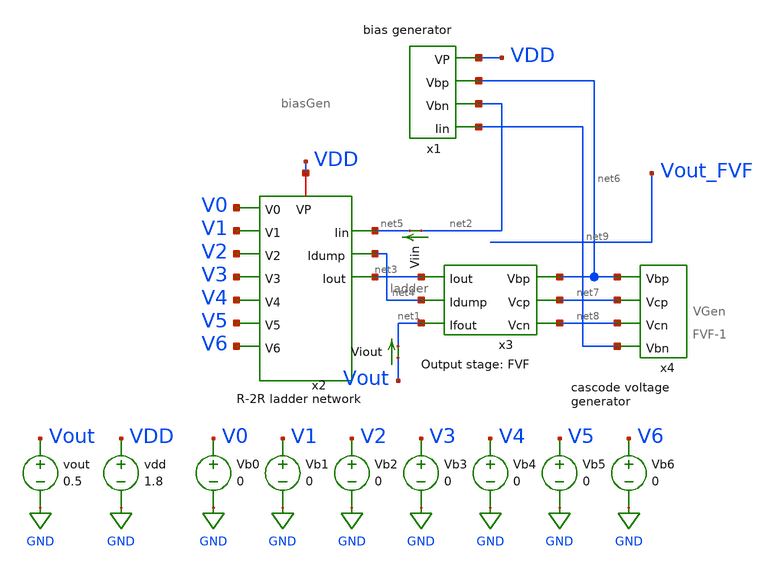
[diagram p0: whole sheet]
** sch_path: xschem/old_files/mp4_dac_simulation_mc.sch
**.subckt mp4_dac_simulation_mc
Vb1 V1 GND 0
Vb2 V2 GND 0
Vb3 V3 GND 0
Vb4 V4 GND 0
Vb5 V5 GND 0
Vb6 V6 GND 0
Vb0 V0 GND 0
vdd VDD GND 1.8
vout Vout GND 0.5
Viout Vout net1 0
.save i(viout)
Viin net2 net5 0
.save i(viin)
x2 V0 VDD net4 net3 net5 V1 V2 V3 V4 V5 V6 ladder
x1 net6 net9 net2 VDD biasGen
x3 net6 net7 net3 net8 net1 net4 FVF-1
x4 net6 net8 net7 net9 VGen
**** begin user architecture code

.option wnflag=1
.param MC_SWITCH=1.0
.lib ~/skywater/skywater-pdk/libraries/sky130_fd_pr_ngspice/latest/models/sky130.lib.spice tt



.control
  set wr_singlescale
  let runs = 10
  let run = 1
  while run <= runs
  set appendwrite = FALSE
  set wr_vecnames
  let code = 0
   while code < 128
    if code eq 0
      let b0 = 0
    else
      let b0 = code % 2
    end
    if floor(code / 2) eq 0
      let b1 = 0
    else
      let b1 = floor(code / 2) % 2
    end
    if floor(code / 4) eq 0
      let b2 = 0
    else
      let b2 = floor(code / 4) % 2
    end
    if floor(code / 8) eq 0
      let b3 = 0
    else
      let b3 = floor(code / 8) % 2
    end
    if floor(code / 16) eq 0
      let b4 = 0
    else
      let b4 = floor(code / 16) % 2
    end
    if floor(code / 32) eq 0
      let b5 = 0
    else
      let b5 = floor(code / 32) % 2
    end
    if floor(code / 64) eq 0
      let b6 = 0
    else
      let b6 = floor(code / 64) % 2
    end
    alter Vb0 1.8*$&b0
    alter Vb1 1.8*$&b1
    alter Vb2 1.8*$&b2
    alter Vb3 1.8*$&b3
    alter Vb4 1.8*$&b4
    alter Vb5 1.8*$&b5
    alter Vb6 1.8*$&b6
    save all
    op
    wrdata ~/Documents/DAC-VLSI/simulation_results/mc/dac_simulation_mc_24_12_{$&run}.txt v(b0) v(b1)
+ v(b2) v(b3) v(b4) v(b5) v(b6) v(Vout_FVF) v(vout) i(Viin) i(Viout)
    if code eq 0
      set appendwrite
      set wr_vecnames = FALSE
    end
    let code = code + 1
  end
  reset
  let run = run + 1
  end
  quit
.endc


**** end user architecture code
**.ends

* expanding   symbol:  ./ladder.sym # of pins=11
** sym_path: xschem/ladder.sym
** sch_path: xschem/ladder.sch
.subckt ladder V0 VP Idump Iout Iin V1 V2 V3 V4 V5 V6
*.ipin V6
*.ipin V5
*.ipin V4
*.ipin V3
*.ipin V2
*.ipin V1
*.ipin V0
*.iopin VP
*.iopin Iin
*.opin Idump
*.opin Iout
XM1 Iin VP net1 GND sky130_fd_pr__nfet_01v8 L=4 W=12 nf=1 ad='int((nf+1)/2) * W/nf * 0.29' as='int((nf+2)/2) * W/nf * 0.29'
+ pd='2*int((nf+1)/2) * (W/nf + 0.29)' ps='2*int((nf+2)/2) * (W/nf + 0.29)' nrd='0.29 / W' nrs='0.29 / W'
+ sa=0 sb=0 sd=0 mult=1 m=1
XM3 Iin VP net2 GND sky130_fd_pr__nfet_01v8 L=4 W=12 nf=1 ad='int((nf+1)/2) * W/nf * 0.29' as='int((nf+2)/2) * W/nf * 0.29'
+ pd='2*int((nf+1)/2) * (W/nf + 0.29)' ps='2*int((nf+2)/2) * (W/nf + 0.29)' nrd='0.29 / W' nrs='0.29 / W'
+ sa=0 sb=0 sd=0 mult=1 m=1
XM5 net2 VP net3 GND sky130_fd_pr__nfet_01v8 L=4 W=12 nf=1 ad='int((nf+1)/2) * W/nf * 0.29' as='int((nf+2)/2) * W/nf * 0.29'
+ pd='2*int((nf+1)/2) * (W/nf + 0.29)' ps='2*int((nf+2)/2) * (W/nf + 0.29)' nrd='0.29 / W' nrs='0.29 / W'
+ sa=0 sb=0 sd=0 mult=1 m=1
XM7 net2 VP net4 GND sky130_fd_pr__nfet_01v8 L=4 W=12 nf=1 ad='int((nf+1)/2) * W/nf * 0.29' as='int((nf+2)/2) * W/nf * 0.29'
+ pd='2*int((nf+1)/2) * (W/nf + 0.29)' ps='2*int((nf+2)/2) * (W/nf + 0.29)' nrd='0.29 / W' nrs='0.29 / W'
+ sa=0 sb=0 sd=0 mult=1 m=1
XM6 net3 V5 Iout GND sky130_fd_pr__nfet_01v8 L=4 W=12 nf=1 ad='int((nf+1)/2) * W/nf * 0.29' as='int((nf+2)/2) * W/nf * 0.29'
+ pd='2*int((nf+1)/2) * (W/nf + 0.29)' ps='2*int((nf+2)/2) * (W/nf + 0.29)' nrd='0.29 / W' nrs='0.29 / W'
+ sa=0 sb=0 sd=0 mult=1 m=1
XM8 net3 net16 Idump GND sky130_fd_pr__nfet_01v8 L=4 W=12 nf=1 ad='int((nf+1)/2) * W/nf * 0.29' as='int((nf+2)/2) * W/nf * 0.29'
+ pd='2*int((nf+1)/2) * (W/nf + 0.29)' ps='2*int((nf+2)/2) * (W/nf + 0.29)' nrd='0.29 / W' nrs='0.29 / W'
+ sa=0 sb=0 sd=0 mult=1 m=1
XM2 net1 V6 Iout GND sky130_fd_pr__nfet_01v8 L=4 W=12 nf=1 ad='int((nf+1)/2) * W/nf * 0.29' as='int((nf+2)/2) * W/nf * 0.29'
+ pd='2*int((nf+1)/2) * (W/nf + 0.29)' ps='2*int((nf+2)/2) * (W/nf + 0.29)' nrd='0.29 / W' nrs='0.29 / W'
+ sa=0 sb=0 sd=0 mult=1 m=1
XM4 net1 net15 Idump GND sky130_fd_pr__nfet_01v8 L=4 W=12 nf=1 ad='int((nf+1)/2) * W/nf * 0.29' as='int((nf+2)/2) * W/nf * 0.29'
+ pd='2*int((nf+1)/2) * (W/nf + 0.29)' ps='2*int((nf+2)/2) * (W/nf + 0.29)' nrd='0.29 / W' nrs='0.29 / W'
+ sa=0 sb=0 sd=0 mult=1 m=1
XM9 net4 VP net5 GND sky130_fd_pr__nfet_01v8 L=4 W=12 nf=1 ad='int((nf+1)/2) * W/nf * 0.29' as='int((nf+2)/2) * W/nf * 0.29'
+ pd='2*int((nf+1)/2) * (W/nf + 0.29)' ps='2*int((nf+2)/2) * (W/nf + 0.29)' nrd='0.29 / W' nrs='0.29 / W'
+ sa=0 sb=0 sd=0 mult=1 m=1
XM11 net4 VP net6 GND sky130_fd_pr__nfet_01v8 L=4 W=12 nf=1 ad='int((nf+1)/2) * W/nf * 0.29' as='int((nf+2)/2) * W/nf * 0.29'
+ pd='2*int((nf+1)/2) * (W/nf + 0.29)' ps='2*int((nf+2)/2) * (W/nf + 0.29)' nrd='0.29 / W' nrs='0.29 / W'
+ sa=0 sb=0 sd=0 mult=1 m=1
XM10 net5 V4 Iout GND sky130_fd_pr__nfet_01v8 L=4 W=12 nf=1 ad='int((nf+1)/2) * W/nf * 0.29' as='int((nf+2)/2) * W/nf * 0.29'
+ pd='2*int((nf+1)/2) * (W/nf + 0.29)' ps='2*int((nf+2)/2) * (W/nf + 0.29)' nrd='0.29 / W' nrs='0.29 / W'
+ sa=0 sb=0 sd=0 mult=1 m=1
XM12 net5 net17 Idump GND sky130_fd_pr__nfet_01v8 L=4 W=12 nf=1 ad='int((nf+1)/2) * W/nf * 0.29' as='int((nf+2)/2) * W/nf * 0.29'
+ pd='2*int((nf+1)/2) * (W/nf + 0.29)' ps='2*int((nf+2)/2) * (W/nf + 0.29)' nrd='0.29 / W' nrs='0.29 / W'
+ sa=0 sb=0 sd=0 mult=1 m=1
XM13 net6 VP net7 GND sky130_fd_pr__nfet_01v8 L=4 W=12 nf=1 ad='int((nf+1)/2) * W/nf * 0.29' as='int((nf+2)/2) * W/nf * 0.29'
+ pd='2*int((nf+1)/2) * (W/nf + 0.29)' ps='2*int((nf+2)/2) * (W/nf + 0.29)' nrd='0.29 / W' nrs='0.29 / W'
+ sa=0 sb=0 sd=0 mult=1 m=1
XM15 net6 VP net8 GND sky130_fd_pr__nfet_01v8 L=4 W=12 nf=1 ad='int((nf+1)/2) * W/nf * 0.29' as='int((nf+2)/2) * W/nf * 0.29'
+ pd='2*int((nf+1)/2) * (W/nf + 0.29)' ps='2*int((nf+2)/2) * (W/nf + 0.29)' nrd='0.29 / W' nrs='0.29 / W'
+ sa=0 sb=0 sd=0 mult=1 m=1
XM14 net7 V3 Iout GND sky130_fd_pr__nfet_01v8 L=4 W=12 nf=1 ad='int((nf+1)/2) * W/nf * 0.29' as='int((nf+2)/2) * W/nf * 0.29'
+ pd='2*int((nf+1)/2) * (W/nf + 0.29)' ps='2*int((nf+2)/2) * (W/nf + 0.29)' nrd='0.29 / W' nrs='0.29 / W'
+ sa=0 sb=0 sd=0 mult=1 m=1
XM16 net7 net18 Idump GND sky130_fd_pr__nfet_01v8 L=4 W=12 nf=1 ad='int((nf+1)/2) * W/nf * 0.29' as='int((nf+2)/2) * W/nf * 0.29'
+ pd='2*int((nf+1)/2) * (W/nf + 0.29)' ps='2*int((nf+2)/2) * (W/nf + 0.29)' nrd='0.29 / W' nrs='0.29 / W'
+ sa=0 sb=0 sd=0 mult=1 m=1
XM17 net8 VP net9 GND sky130_fd_pr__nfet_01v8 L=4 W=12 nf=1 ad='int((nf+1)/2) * W/nf * 0.29' as='int((nf+2)/2) * W/nf * 0.29'
+ pd='2*int((nf+1)/2) * (W/nf + 0.29)' ps='2*int((nf+2)/2) * (W/nf + 0.29)' nrd='0.29 / W' nrs='0.29 / W'
+ sa=0 sb=0 sd=0 mult=1 m=1
XM19 net8 VP net10 GND sky130_fd_pr__nfet_01v8 L=4 W=12 nf=1 ad='int((nf+1)/2) * W/nf * 0.29' as='int((nf+2)/2) * W/nf * 0.29'
+ pd='2*int((nf+1)/2) * (W/nf + 0.29)' ps='2*int((nf+2)/2) * (W/nf + 0.29)' nrd='0.29 / W' nrs='0.29 / W'
+ sa=0 sb=0 sd=0 mult=1 m=1
XM18 net9 V2 Iout GND sky130_fd_pr__nfet_01v8 L=4 W=12 nf=1 ad='int((nf+1)/2) * W/nf * 0.29' as='int((nf+2)/2) * W/nf * 0.29'
+ pd='2*int((nf+1)/2) * (W/nf + 0.29)' ps='2*int((nf+2)/2) * (W/nf + 0.29)' nrd='0.29 / W' nrs='0.29 / W'
+ sa=0 sb=0 sd=0 mult=1 m=1
XM20 net9 net19 Idump GND sky130_fd_pr__nfet_01v8 L=4 W=12 nf=1 ad='int((nf+1)/2) * W/nf * 0.29' as='int((nf+2)/2) * W/nf * 0.29'
+ pd='2*int((nf+1)/2) * (W/nf + 0.29)' ps='2*int((nf+2)/2) * (W/nf + 0.29)' nrd='0.29 / W' nrs='0.29 / W'
+ sa=0 sb=0 sd=0 mult=1 m=1
XM21 net10 VP net11 GND sky130_fd_pr__nfet_01v8 L=4 W=12 nf=1 ad='int((nf+1)/2) * W/nf * 0.29' as='int((nf+2)/2) * W/nf * 0.29'
+ pd='2*int((nf+1)/2) * (W/nf + 0.29)' ps='2*int((nf+2)/2) * (W/nf + 0.29)' nrd='0.29 / W' nrs='0.29 / W'
+ sa=0 sb=0 sd=0 mult=1 m=1
XM23 net10 VP net12 GND sky130_fd_pr__nfet_01v8 L=4 W=12 nf=1 ad='int((nf+1)/2) * W/nf * 0.29' as='int((nf+2)/2) * W/nf * 0.29'
+ pd='2*int((nf+1)/2) * (W/nf + 0.29)' ps='2*int((nf+2)/2) * (W/nf + 0.29)' nrd='0.29 / W' nrs='0.29 / W'
+ sa=0 sb=0 sd=0 mult=1 m=1
XM22 net11 V1 Iout GND sky130_fd_pr__nfet_01v8 L=4 W=12 nf=1 ad='int((nf+1)/2) * W/nf * 0.29' as='int((nf+2)/2) * W/nf * 0.29'
+ pd='2*int((nf+1)/2) * (W/nf + 0.29)' ps='2*int((nf+2)/2) * (W/nf + 0.29)' nrd='0.29 / W' nrs='0.29 / W'
+ sa=0 sb=0 sd=0 mult=1 m=1
XM24 net11 net20 Idump GND sky130_fd_pr__nfet_01v8 L=4 W=12 nf=1 ad='int((nf+1)/2) * W/nf * 0.29' as='int((nf+2)/2) * W/nf * 0.29'
+ pd='2*int((nf+1)/2) * (W/nf + 0.29)' ps='2*int((nf+2)/2) * (W/nf + 0.29)' nrd='0.29 / W' nrs='0.29 / W'
+ sa=0 sb=0 sd=0 mult=1 m=1
XM25 net12 VP net13 GND sky130_fd_pr__nfet_01v8 L=4 W=12 nf=1 ad='int((nf+1)/2) * W/nf * 0.29' as='int((nf+2)/2) * W/nf * 0.29'
+ pd='2*int((nf+1)/2) * (W/nf + 0.29)' ps='2*int((nf+2)/2) * (W/nf + 0.29)' nrd='0.29 / W' nrs='0.29 / W'
+ sa=0 sb=0 sd=0 mult=1 m=1
XM27 net12 VP net14 GND sky130_fd_pr__nfet_01v8 L=4 W=12 nf=1 ad='int((nf+1)/2) * W/nf * 0.29' as='int((nf+2)/2) * W/nf * 0.29'
+ pd='2*int((nf+1)/2) * (W/nf + 0.29)' ps='2*int((nf+2)/2) * (W/nf + 0.29)' nrd='0.29 / W' nrs='0.29 / W'
+ sa=0 sb=0 sd=0 mult=1 m=1
XM26 net13 V0 Iout GND sky130_fd_pr__nfet_01v8 L=4 W=12 nf=1 ad='int((nf+1)/2) * W/nf * 0.29' as='int((nf+2)/2) * W/nf * 0.29'
+ pd='2*int((nf+1)/2) * (W/nf + 0.29)' ps='2*int((nf+2)/2) * (W/nf + 0.29)' nrd='0.29 / W' nrs='0.29 / W'
+ sa=0 sb=0 sd=0 mult=1 m=1
XM28 net13 net21 Idump GND sky130_fd_pr__nfet_01v8 L=4 W=12 nf=1 ad='int((nf+1)/2) * W/nf * 0.29' as='int((nf+2)/2) * W/nf * 0.29'
+ pd='2*int((nf+1)/2) * (W/nf + 0.29)' ps='2*int((nf+2)/2) * (W/nf + 0.29)' nrd='0.29 / W' nrs='0.29 / W'
+ sa=0 sb=0 sd=0 mult=1 m=1
XM29 net14 VP Idump GND sky130_fd_pr__nfet_01v8 L=4 W=12 nf=1 ad='int((nf+1)/2) * W/nf * 0.29' as='int((nf+2)/2) * W/nf * 0.29'
+ pd='2*int((nf+1)/2) * (W/nf + 0.29)' ps='2*int((nf+2)/2) * (W/nf + 0.29)' nrd='0.29 / W' nrs='0.29 / W'
+ sa=0 sb=0 sd=0 mult=1 m=1
x1 net15 V6 inverter
x2 net16 V5 inverter
x3 net17 V4 inverter
x4 net18 V3 inverter
x5 net19 V2 inverter
x6 net20 V1 inverter
x7 net21 V0 inverter
.ends


* expanding   symbol:  /home/madvlsi/Documents/DAC-VLSI/xschem/biasGen.sym # of pins=4
** sym_path: xschem/biasGen.sym
** sch_path: xschem/biasGen.sch
.subckt biasGen Vbp Iin Vbn VP
*.opin Iin
*.ipin VP
*.opin Vbp
*.opin Vbn
XM1 Vbn Vbn GND GND sky130_fd_pr__nfet_01v8 L=4 W=24 nf=1 ad='int((nf+1)/2) * W/nf * 0.29' as='int((nf+2)/2) * W/nf * 0.29'
+ pd='2*int((nf+1)/2) * (W/nf + 0.29)' ps='2*int((nf+2)/2) * (W/nf + 0.29)' nrd='0.29 / W' nrs='0.29 / W'
+ sa=0 sb=0 sd=0 mult=1 m=1
XM2 GND Vbn Vbp GND sky130_fd_pr__nfet_01v8 L=4 W=24 nf=1 ad='int((nf+1)/2) * W/nf * 0.29' as='int((nf+2)/2) * W/nf * 0.29'
+ pd='2*int((nf+1)/2) * (W/nf + 0.29)' ps='2*int((nf+2)/2) * (W/nf + 0.29)' nrd='0.29 / W' nrs='0.29 / W'
+ sa=0 sb=0 sd=0 mult=1 m=1
XM3 net1 net2 GND GND sky130_fd_pr__nfet_01v8 L=4 W=24 nf=1 ad='int((nf+1)/2) * W/nf * 0.29' as='int((nf+2)/2) * W/nf * 0.29'
+ pd='2*int((nf+1)/2) * (W/nf + 0.29)' ps='2*int((nf+2)/2) * (W/nf + 0.29)' nrd='0.29 / W' nrs='0.29 / W'
+ sa=0 sb=0 sd=0 mult=1 m=1
XM4 net13 net2 net2 GND sky130_fd_pr__nfet_01v8 L=4 W=24 nf=1 ad='int((nf+1)/2) * W/nf * 0.29' as='int((nf+2)/2) * W/nf * 0.29'
+ pd='2*int((nf+1)/2) * (W/nf + 0.29)' ps='2*int((nf+2)/2) * (W/nf + 0.29)' nrd='0.29 / W' nrs='0.29 / W'
+ sa=0 sb=0 sd=0 mult=8 m=8
XM5 Vbp net1 net5 VDD sky130_fd_pr__pfet_01v8 L=4 W=24 nf=1 ad='int((nf+1)/2) * W/nf * 0.29' as='int((nf+2)/2) * W/nf * 0.29'
+ pd='2*int((nf+1)/2) * (W/nf + 0.29)' ps='2*int((nf+2)/2) * (W/nf + 0.29)' nrd='0.29 / W' nrs='0.29 / W'
+ sa=0 sb=0 sd=0 mult=1 m=1
XM6 net6 net1 net1 VDD sky130_fd_pr__pfet_01v8 L=4 W=24 nf=1 ad='int((nf+1)/2) * W/nf * 0.29' as='int((nf+2)/2) * W/nf * 0.29'
+ pd='2*int((nf+1)/2) * (W/nf + 0.29)' ps='2*int((nf+2)/2) * (W/nf + 0.29)' nrd='0.29 / W' nrs='0.29 / W'
+ sa=0 sb=0 sd=0 mult=1 m=1
XM7 net3 Vbp net2 VDD sky130_fd_pr__pfet_01v8 L=4 W=24 nf=1 ad='int((nf+1)/2) * W/nf * 0.29' as='int((nf+2)/2) * W/nf * 0.29'
+ pd='2*int((nf+1)/2) * (W/nf + 0.29)' ps='2*int((nf+2)/2) * (W/nf + 0.29)' nrd='0.29 / W' nrs='0.29 / W'
+ sa=0 sb=0 sd=0 mult=1 m=1
XM8 Vbn Vbp net4 VDD sky130_fd_pr__pfet_01v8 L=4 W=24 nf=1 ad='int((nf+1)/2) * W/nf * 0.29' as='int((nf+2)/2) * W/nf * 0.29'
+ pd='2*int((nf+1)/2) * (W/nf + 0.29)' ps='2*int((nf+2)/2) * (W/nf + 0.29)' nrd='0.29 / W' nrs='0.29 / W'
+ sa=0 sb=0 sd=0 mult=1 m=1
R1 net13 GND 90K m=1
XM9 Iin Vbp net7 VDD sky130_fd_pr__pfet_01v8 L=4 W=24 nf=1 ad='int((nf+1)/2) * W/nf * 0.29' as='int((nf+2)/2) * W/nf * 0.29'
+ pd='2*int((nf+1)/2) * (W/nf + 0.29)' ps='2*int((nf+2)/2) * (W/nf + 0.29)' nrd='0.29 / W' nrs='0.29 / W'
+ sa=0 sb=0 sd=0 mult=1 m=1
XM10 net8 Vbp net3 VDD sky130_fd_pr__pfet_01v8 L=4 W=24 nf=1 ad='int((nf+1)/2) * W/nf * 0.29' as='int((nf+2)/2) * W/nf * 0.29'
+ pd='2*int((nf+1)/2) * (W/nf + 0.29)' ps='2*int((nf+2)/2) * (W/nf + 0.29)' nrd='0.29 / W' nrs='0.29 / W'
+ sa=0 sb=0 sd=0 mult=1 m=1
XM11 net12 net1 net6 VDD sky130_fd_pr__pfet_01v8 L=4 W=24 nf=1 ad='int((nf+1)/2) * W/nf * 0.29' as='int((nf+2)/2) * W/nf * 0.29'
+ pd='2*int((nf+1)/2) * (W/nf + 0.29)' ps='2*int((nf+2)/2) * (W/nf + 0.29)' nrd='0.29 / W' nrs='0.29 / W'
+ sa=0 sb=0 sd=0 mult=1 m=1
XM12 net11 net1 net5 VDD sky130_fd_pr__pfet_01v8 L=4 W=24 nf=1 ad='int((nf+1)/2) * W/nf * 0.29' as='int((nf+2)/2) * W/nf * 0.29'
+ pd='2*int((nf+1)/2) * (W/nf + 0.29)' ps='2*int((nf+2)/2) * (W/nf + 0.29)' nrd='0.29 / W' nrs='0.29 / W'
+ sa=0 sb=0 sd=0 mult=1 m=1
XM13 net10 Vbp net4 VDD sky130_fd_pr__pfet_01v8 L=4 W=24 nf=1 ad='int((nf+1)/2) * W/nf * 0.29' as='int((nf+2)/2) * W/nf * 0.29'
+ pd='2*int((nf+1)/2) * (W/nf + 0.29)' ps='2*int((nf+2)/2) * (W/nf + 0.29)' nrd='0.29 / W' nrs='0.29 / W'
+ sa=0 sb=0 sd=0 mult=1 m=1
XM14 net9 Vbp net7 VDD sky130_fd_pr__pfet_01v8 L=4 W=24 nf=1 ad='int((nf+1)/2) * W/nf * 0.29' as='int((nf+2)/2) * W/nf * 0.29'
+ pd='2*int((nf+1)/2) * (W/nf + 0.29)' ps='2*int((nf+2)/2) * (W/nf + 0.29)' nrd='0.29 / W' nrs='0.29 / W'
+ sa=0 sb=0 sd=0 mult=1 m=1
XM15 VP Vbp net8 VDD sky130_fd_pr__pfet_01v8 L=4 W=24 nf=1 ad='int((nf+1)/2) * W/nf * 0.29' as='int((nf+2)/2) * W/nf * 0.29'
+ pd='2*int((nf+1)/2) * (W/nf + 0.29)' ps='2*int((nf+2)/2) * (W/nf + 0.29)' nrd='0.29 / W' nrs='0.29 / W'
+ sa=0 sb=0 sd=0 mult=1 m=1
XM16 VP net1 net12 VDD sky130_fd_pr__pfet_01v8 L=4 W=24 nf=1 ad='int((nf+1)/2) * W/nf * 0.29' as='int((nf+2)/2) * W/nf * 0.29'
+ pd='2*int((nf+1)/2) * (W/nf + 0.29)' ps='2*int((nf+2)/2) * (W/nf + 0.29)' nrd='0.29 / W' nrs='0.29 / W'
+ sa=0 sb=0 sd=0 mult=1 m=1
XM17 VP net1 net11 VDD sky130_fd_pr__pfet_01v8 L=4 W=24 nf=1 ad='int((nf+1)/2) * W/nf * 0.29' as='int((nf+2)/2) * W/nf * 0.29'
+ pd='2*int((nf+1)/2) * (W/nf + 0.29)' ps='2*int((nf+2)/2) * (W/nf + 0.29)' nrd='0.29 / W' nrs='0.29 / W'
+ sa=0 sb=0 sd=0 mult=1 m=1
XM18 VP Vbp net10 VDD sky130_fd_pr__pfet_01v8 L=4 W=24 nf=1 ad='int((nf+1)/2) * W/nf * 0.29' as='int((nf+2)/2) * W/nf * 0.29'
+ pd='2*int((nf+1)/2) * (W/nf + 0.29)' ps='2*int((nf+2)/2) * (W/nf + 0.29)' nrd='0.29 / W' nrs='0.29 / W'
+ sa=0 sb=0 sd=0 mult=1 m=1
XM19 VP Vbp net9 VDD sky130_fd_pr__pfet_01v8 L=4 W=24 nf=1 ad='int((nf+1)/2) * W/nf * 0.29' as='int((nf+2)/2) * W/nf * 0.29'
+ pd='2*int((nf+1)/2) * (W/nf + 0.29)' ps='2*int((nf+2)/2) * (W/nf + 0.29)' nrd='0.29 / W' nrs='0.29 / W'
+ sa=0 sb=0 sd=0 mult=1 m=1
.ends


* expanding   symbol:  /home/madvlsi/Documents/DAC-VLSI/xschem/FVF-1.sym # of pins=6
** sym_path: xschem/FVF-1.sym
** sch_path: xschem/FVF-1.sch
.subckt FVF-1 Vbp Vcp Iout Vcn Ifout Idump
*.ipin Vcn
*.ipin Iout
*.ipin Idump
*.ipin Vcp
*.ipin Vbp
*.opin Ifout
XM1 net1 Vcn Idump GND sky130_fd_pr__nfet_01v8 L=4 W=24 nf=1 ad='int((nf+1)/2) * W/nf * 0.29' as='int((nf+2)/2) * W/nf * 0.29'
+ pd='2*int((nf+1)/2) * (W/nf + 0.29)' ps='2*int((nf+2)/2) * (W/nf + 0.29)' nrd='0.29 / W' nrs='0.29 / W'
+ sa=0 sb=0 sd=0 mult=1 m=1
XM2 GND net1 Idump GND sky130_fd_pr__nfet_01v8 L=4 W=24 nf=1 ad='int((nf+1)/2) * W/nf * 0.29' as='int((nf+2)/2) * W/nf * 0.29'
+ pd='2*int((nf+1)/2) * (W/nf + 0.29)' ps='2*int((nf+2)/2) * (W/nf + 0.29)' nrd='0.29 / W' nrs='0.29 / W'
+ sa=0 sb=0 sd=0 mult=1 m=1
XM3 net2 Vcn Iout GND sky130_fd_pr__nfet_01v8 L=4 W=24 nf=1 ad='int((nf+1)/2) * W/nf * 0.29' as='int((nf+2)/2) * W/nf * 0.29'
+ pd='2*int((nf+1)/2) * (W/nf + 0.29)' ps='2*int((nf+2)/2) * (W/nf + 0.29)' nrd='0.29 / W' nrs='0.29 / W'
+ sa=0 sb=0 sd=0 mult=1 m=1
XM4 GND net2 Iout GND sky130_fd_pr__nfet_01v8 L=4 W=24 nf=1 ad='int((nf+1)/2) * W/nf * 0.29' as='int((nf+2)/2) * W/nf * 0.29'
+ pd='2*int((nf+1)/2) * (W/nf + 0.29)' ps='2*int((nf+2)/2) * (W/nf + 0.29)' nrd='0.29 / W' nrs='0.29 / W'
+ sa=0 sb=0 sd=0 mult=1 m=1
XM5 Ifout Vcn net3 GND sky130_fd_pr__nfet_01v8 L=4 W=24 nf=1 ad='int((nf+1)/2) * W/nf * 0.29' as='int((nf+2)/2) * W/nf * 0.29'
+ pd='2*int((nf+1)/2) * (W/nf + 0.29)' ps='2*int((nf+2)/2) * (W/nf + 0.29)' nrd='0.29 / W' nrs='0.29 / W'
+ sa=0 sb=0 sd=0 mult=1 m=1
XM6 net3 net2 GND GND sky130_fd_pr__nfet_01v8 L=4 W=24 nf=1 ad='int((nf+1)/2) * W/nf * 0.29' as='int((nf+2)/2) * W/nf * 0.29'
+ pd='2*int((nf+1)/2) * (W/nf + 0.29)' ps='2*int((nf+2)/2) * (W/nf + 0.29)' nrd='0.29 / W' nrs='0.29 / W'
+ sa=0 sb=0 sd=0 mult=1 m=1
XM7 net1 Vcp net4 VDD sky130_fd_pr__pfet_01v8 L=8 W=24 nf=1 ad='int((nf+1)/2) * W/nf * 0.29' as='int((nf+2)/2) * W/nf * 0.29'
+ pd='2*int((nf+1)/2) * (W/nf + 0.29)' ps='2*int((nf+2)/2) * (W/nf + 0.29)' nrd='0.29 / W' nrs='0.29 / W'
+ sa=0 sb=0 sd=0 mult=1 m=1
XM8 net2 Vcp net5 VDD sky130_fd_pr__pfet_01v8 L=8 W=24 nf=1 ad='int((nf+1)/2) * W/nf * 0.29' as='int((nf+2)/2) * W/nf * 0.29'
+ pd='2*int((nf+1)/2) * (W/nf + 0.29)' ps='2*int((nf+2)/2) * (W/nf + 0.29)' nrd='0.29 / W' nrs='0.29 / W'
+ sa=0 sb=0 sd=0 mult=1 m=1
XM9 Ifout Vcp net6 VDD sky130_fd_pr__pfet_01v8 L=8 W=24 nf=1 ad='int((nf+1)/2) * W/nf * 0.29' as='int((nf+2)/2) * W/nf * 0.29'
+ pd='2*int((nf+1)/2) * (W/nf + 0.29)' ps='2*int((nf+2)/2) * (W/nf + 0.29)' nrd='0.29 / W' nrs='0.29 / W'
+ sa=0 sb=0 sd=0 mult=1 m=1
XM15 net4 Vbp VDD VDD sky130_fd_pr__pfet_01v8 L=8 W=24 nf=1 ad='int((nf+1)/2) * W/nf * 0.29' as='int((nf+2)/2) * W/nf * 0.29'
+ pd='2*int((nf+1)/2) * (W/nf + 0.29)' ps='2*int((nf+2)/2) * (W/nf + 0.29)' nrd='0.29 / W' nrs='0.29 / W'
+ sa=0 sb=0 sd=0 mult=1 m=1
XM16 net5 Vbp VDD VDD sky130_fd_pr__pfet_01v8 L=8 W=24 nf=1 ad='int((nf+1)/2) * W/nf * 0.29' as='int((nf+2)/2) * W/nf * 0.29'
+ pd='2*int((nf+1)/2) * (W/nf + 0.29)' ps='2*int((nf+2)/2) * (W/nf + 0.29)' nrd='0.29 / W' nrs='0.29 / W'
+ sa=0 sb=0 sd=0 mult=1 m=1
XM17 net6 Vbp VDD VDD sky130_fd_pr__pfet_01v8 L=8 W=24 nf=1 ad='int((nf+1)/2) * W/nf * 0.29' as='int((nf+2)/2) * W/nf * 0.29'
+ pd='2*int((nf+1)/2) * (W/nf + 0.29)' ps='2*int((nf+2)/2) * (W/nf + 0.29)' nrd='0.29 / W' nrs='0.29 / W'
+ sa=0 sb=0 sd=0 mult=1 m=1
.ends


* expanding   symbol:  /home/madvlsi/Documents/DAC-VLSI/xschem/VGen.sym # of pins=4
** sym_path: xschem/VGen.sym
** sch_path: xschem/VGen.sch
.subckt VGen Vbp Vcn Vcp Vbn
*.opin Vcp
*.ipin Vbp
*.ipin Vbn
*.opin Vcn
XM5 net4 net4 net1 GND sky130_fd_pr__nfet_01v8 L=8 W=96 nf=1 ad='int((nf+1)/2) * W/nf * 0.29' as='int((nf+2)/2) * W/nf * 0.29'
+ pd='2*int((nf+1)/2) * (W/nf + 0.29)' ps='2*int((nf+2)/2) * (W/nf + 0.29)' nrd='0.29 / W' nrs='0.29 / W'
+ sa=0 sb=0 sd=0 mult=1 m=1
XM6 net1 net4 GND GND sky130_fd_pr__nfet_01v8 L=8 W=24 nf=1 ad='int((nf+1)/2) * W/nf * 0.29' as='int((nf+2)/2) * W/nf * 0.29'
+ pd='2*int((nf+1)/2) * (W/nf + 0.29)' ps='2*int((nf+2)/2) * (W/nf + 0.29)' nrd='0.29 / W' nrs='0.29 / W'
+ sa=0 sb=0 sd=0 mult=1 m=1
XM4 net1 Vcn Vcn GND sky130_fd_pr__nfet_01v8 L=8 W=24 nf=1 ad='int((nf+1)/2) * W/nf * 0.29' as='int((nf+2)/2) * W/nf * 0.29'
+ pd='2*int((nf+1)/2) * (W/nf + 0.29)' ps='2*int((nf+2)/2) * (W/nf + 0.29)' nrd='0.29 / W' nrs='0.29 / W'
+ sa=0 sb=0 sd=0 mult=1 m=1
XM1 VDD Vbp net4 VDD sky130_fd_pr__pfet_01v8 L=32 W=24 nf=1 ad='int((nf+1)/2) * W/nf * 0.29' as='int((nf+2)/2) * W/nf * 0.29'
+ pd='2*int((nf+1)/2) * (W/nf + 0.29)' ps='2*int((nf+2)/2) * (W/nf + 0.29)' nrd='0.29 / W' nrs='0.29 / W'
+ sa=0 sb=0 sd=0 mult=1 m=1
XM2 VDD Vbp Vcn VDD sky130_fd_pr__pfet_01v8 L=8 W=24 nf=1 ad='int((nf+1)/2) * W/nf * 0.29' as='int((nf+2)/2) * W/nf * 0.29'
+ pd='2*int((nf+1)/2) * (W/nf + 0.29)' ps='2*int((nf+2)/2) * (W/nf + 0.29)' nrd='0.29 / W' nrs='0.29 / W'
+ sa=0 sb=0 sd=0 mult=1 m=1
XM9 net3 net3 net2 VDD sky130_fd_pr__pfet_01v8 L=8 W=96 nf=1 ad='int((nf+1)/2) * W/nf * 0.29' as='int((nf+2)/2) * W/nf * 0.29'
+ pd='2*int((nf+1)/2) * (W/nf + 0.29)' ps='2*int((nf+2)/2) * (W/nf + 0.29)' nrd='0.29 / W' nrs='0.29 / W'
+ sa=0 sb=0 sd=0 mult=1 m=1
XM11 GND Vbn Vcp GND sky130_fd_pr__nfet_01v8 L=8 W=24 nf=1 ad='int((nf+1)/2) * W/nf * 0.29' as='int((nf+2)/2) * W/nf * 0.29'
+ pd='2*int((nf+1)/2) * (W/nf + 0.29)' ps='2*int((nf+2)/2) * (W/nf + 0.29)' nrd='0.29 / W' nrs='0.29 / W'
+ sa=0 sb=0 sd=0 mult=1 m=1
XM8 net2 Vcp Vcp VDD sky130_fd_pr__pfet_01v8 L=8 W=24 nf=1 ad='int((nf+1)/2) * W/nf * 0.29' as='int((nf+2)/2) * W/nf * 0.29'
+ pd='2*int((nf+1)/2) * (W/nf + 0.29)' ps='2*int((nf+2)/2) * (W/nf + 0.29)' nrd='0.29 / W' nrs='0.29 / W'
+ sa=0 sb=0 sd=0 mult=1 m=1
XM12 GND Vbn net3 GND sky130_fd_pr__nfet_01v8 L=32 W=24 nf=1 ad='int((nf+1)/2) * W/nf * 0.29' as='int((nf+2)/2) * W/nf * 0.29'
+ pd='2*int((nf+1)/2) * (W/nf + 0.29)' ps='2*int((nf+2)/2) * (W/nf + 0.29)' nrd='0.29 / W' nrs='0.29 / W'
+ sa=0 sb=0 sd=0 mult=1 m=1
XM7 net2 net3 VDD VDD sky130_fd_pr__pfet_01v8 L=8 W=24 nf=1 ad='int((nf+1)/2) * W/nf * 0.29' as='int((nf+2)/2) * W/nf * 0.29'
+ pd='2*int((nf+1)/2) * (W/nf + 0.29)' ps='2*int((nf+2)/2) * (W/nf + 0.29)' nrd='0.29 / W' nrs='0.29 / W'
+ sa=0 sb=0 sd=0 mult=1 m=1
.ends


* expanding   symbol:  ./inverter.sym # of pins=2
** sym_path: xschem/old_files/inverter.sym
** sch_path: xschem/old_files/inverter.sch
.subckt inverter Y A
*.ipin A
*.opin Y
XM1 Y A VDD VDD sky130_fd_pr__pfet_01v8 L=0.15 W=1 nf=1 ad='int((nf+1)/2) * W/nf * 0.29' as='int((nf+2)/2) * W/nf * 0.29'
+ pd='2*int((nf+1)/2) * (W/nf + 0.29)' ps='2*int((nf+2)/2) * (W/nf + 0.29)' nrd='0.29 / W' nrs='0.29 / W'
+ sa=0 sb=0 sd=0 mult=1 m=1
XM2 Y A GND GND sky130_fd_pr__nfet_01v8 L=0.15 W=1 nf=1 ad='int((nf+1)/2) * W/nf * 0.29' as='int((nf+2)/2) * W/nf * 0.29'
+ pd='2*int((nf+1)/2) * (W/nf + 0.29)' ps='2*int((nf+2)/2) * (W/nf + 0.29)' nrd='0.29 / W' nrs='0.29 / W'
+ sa=0 sb=0 sd=0 mult=1 m=1
.ends

.GLOBAL GND
.GLOBAL VDD
.end
